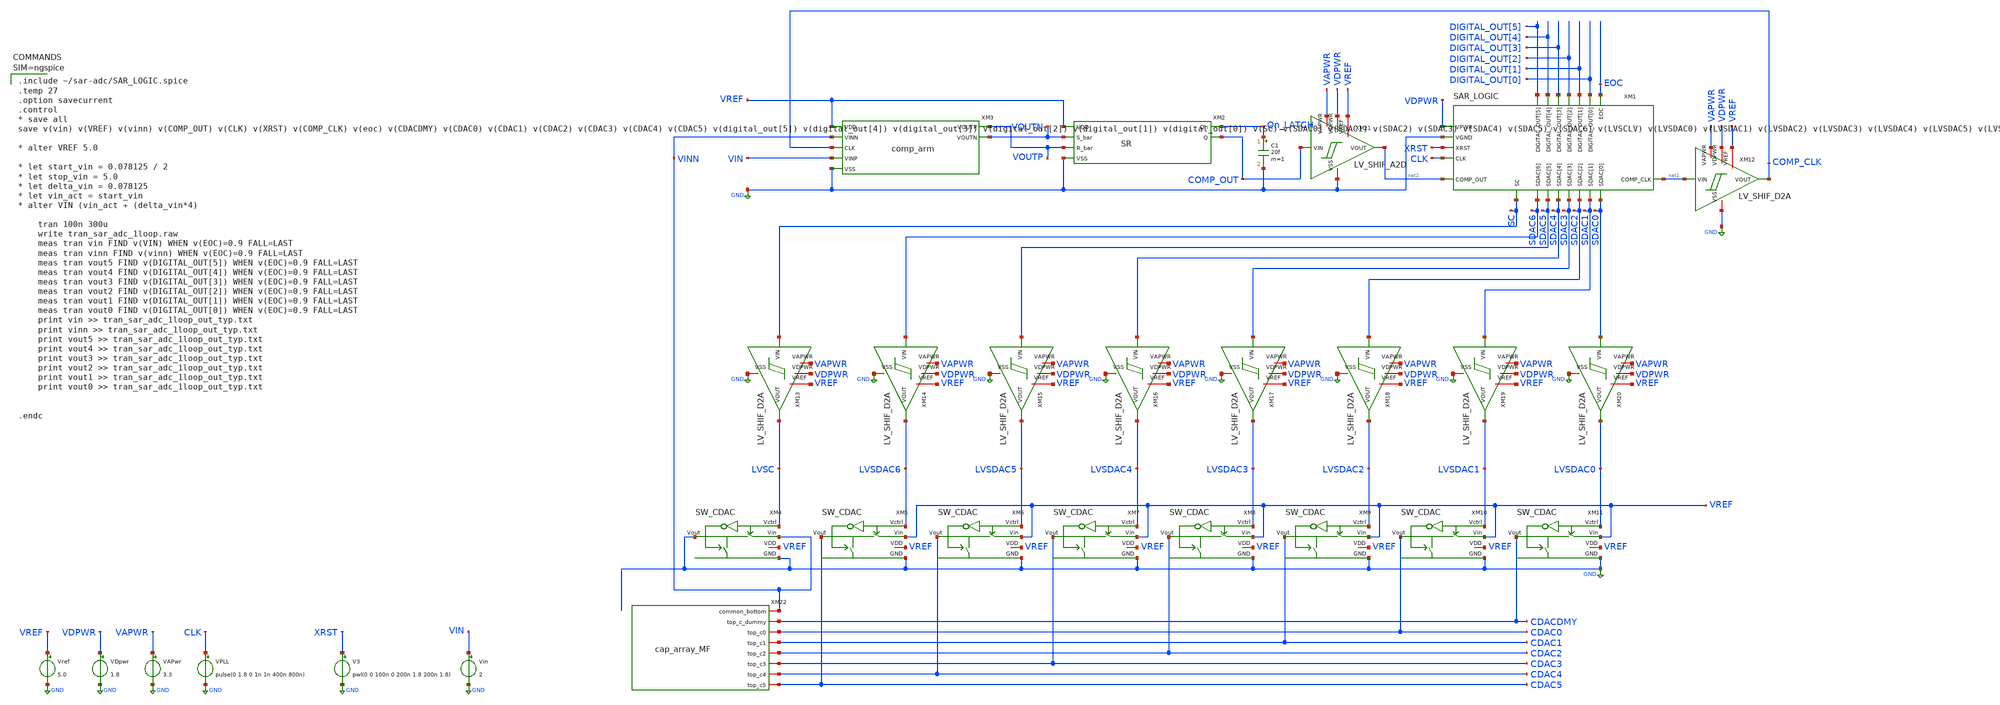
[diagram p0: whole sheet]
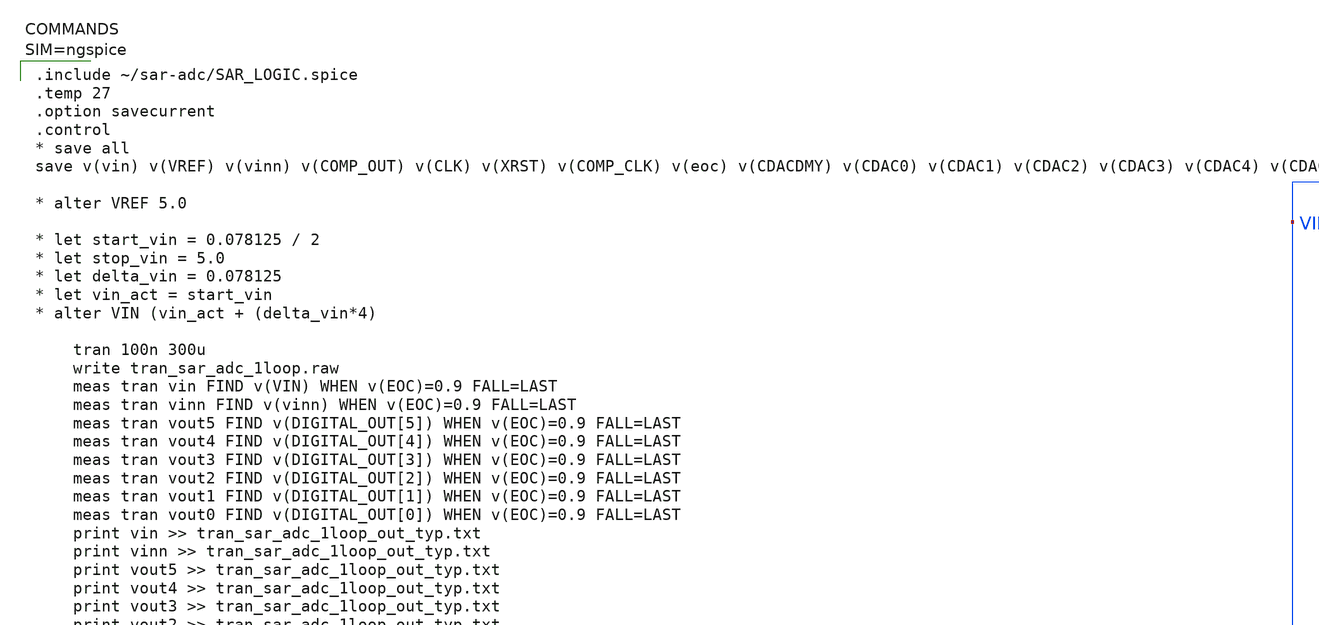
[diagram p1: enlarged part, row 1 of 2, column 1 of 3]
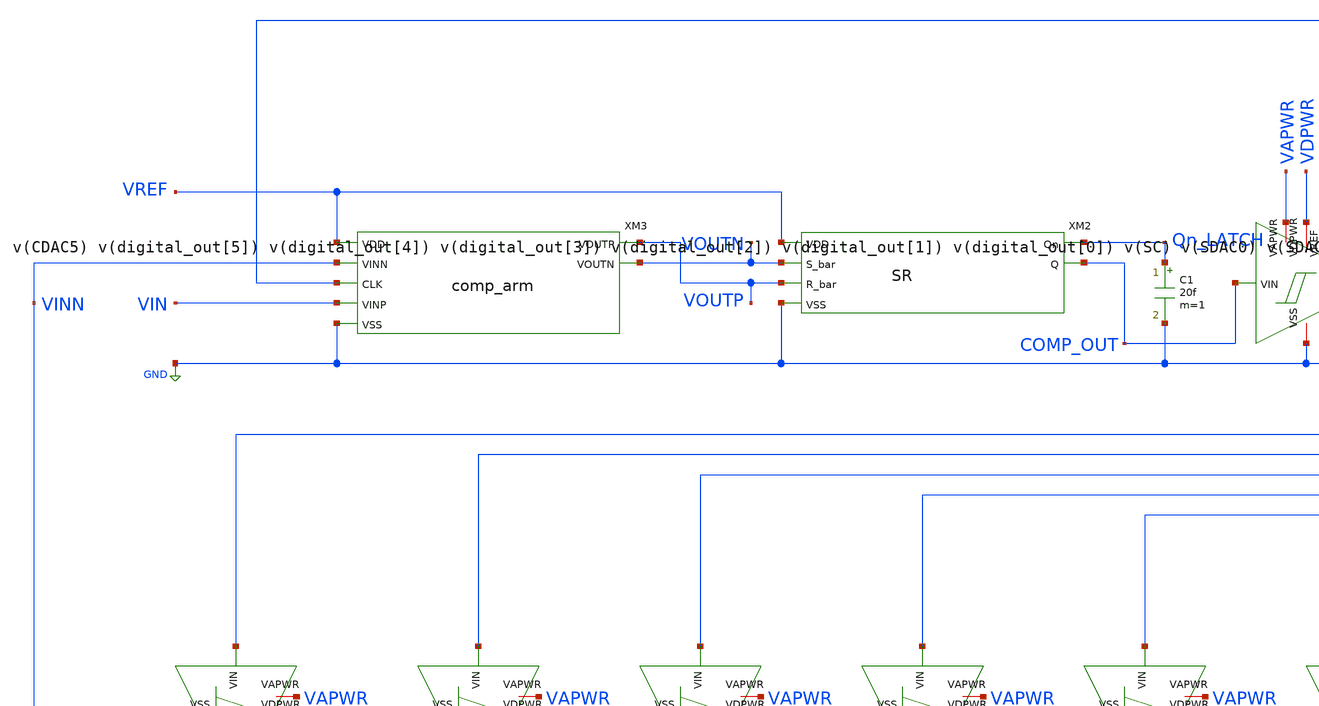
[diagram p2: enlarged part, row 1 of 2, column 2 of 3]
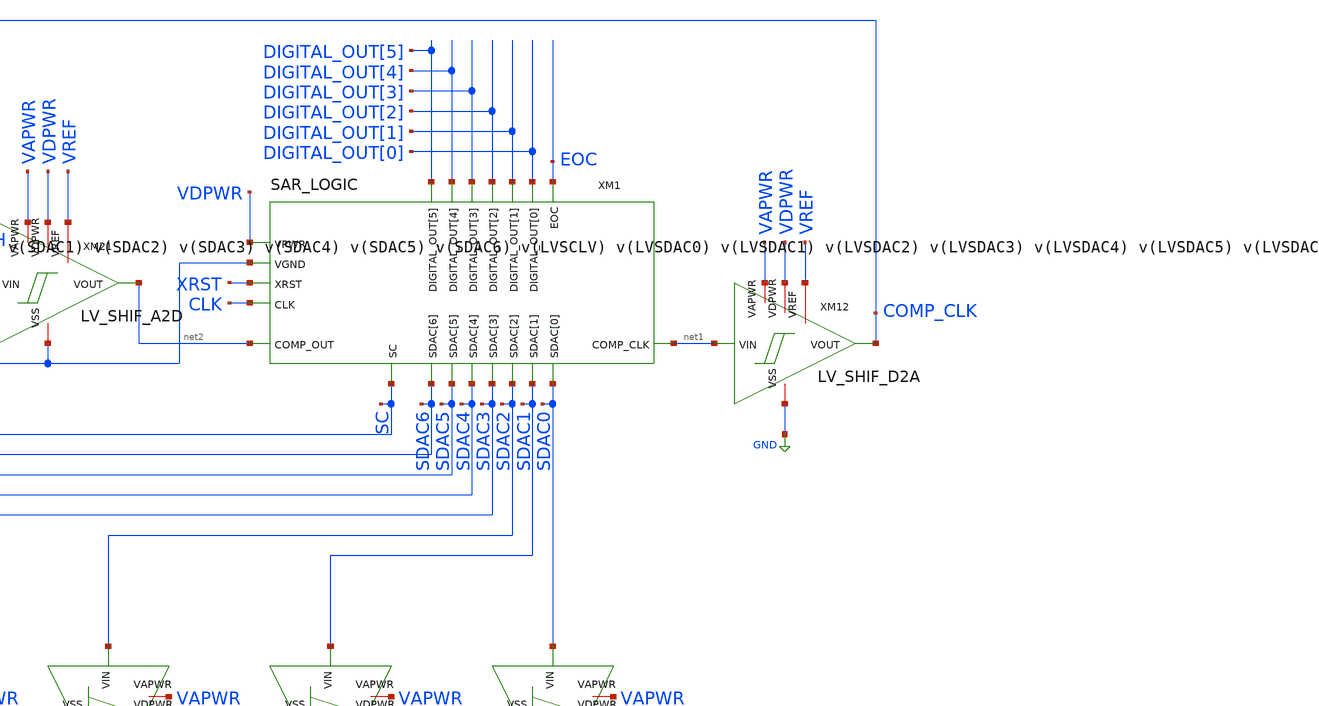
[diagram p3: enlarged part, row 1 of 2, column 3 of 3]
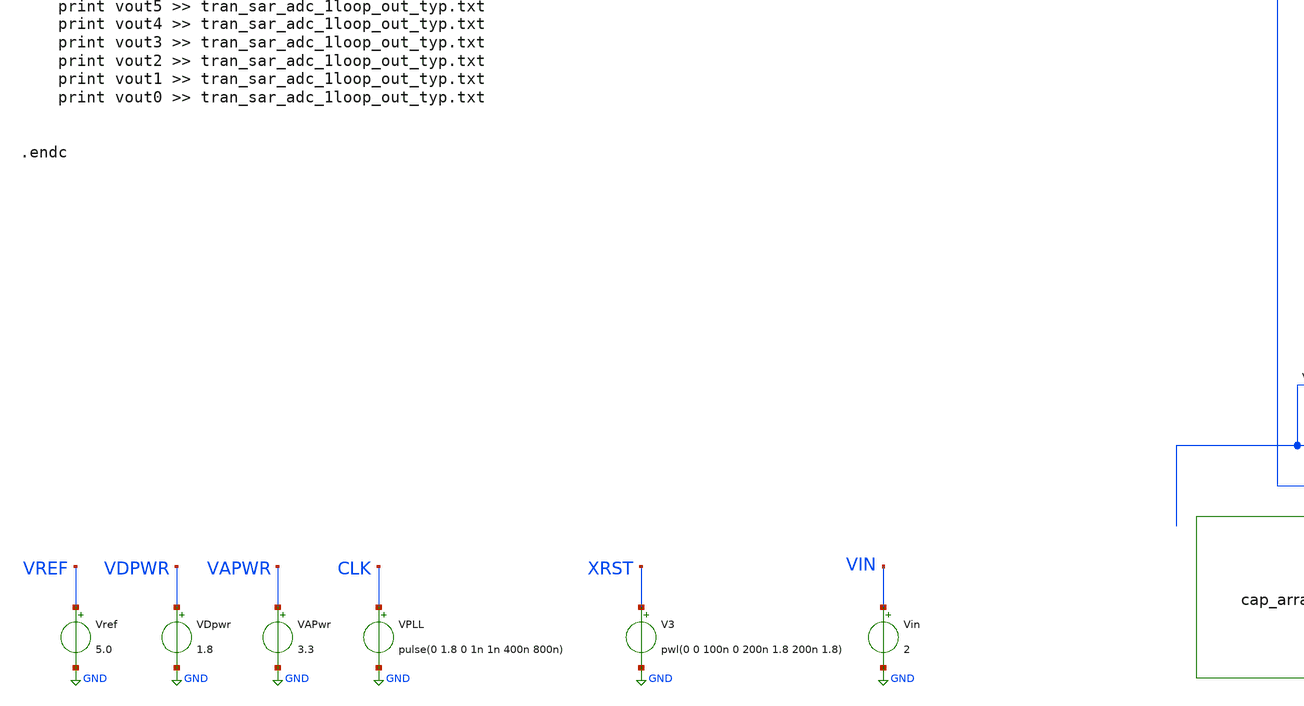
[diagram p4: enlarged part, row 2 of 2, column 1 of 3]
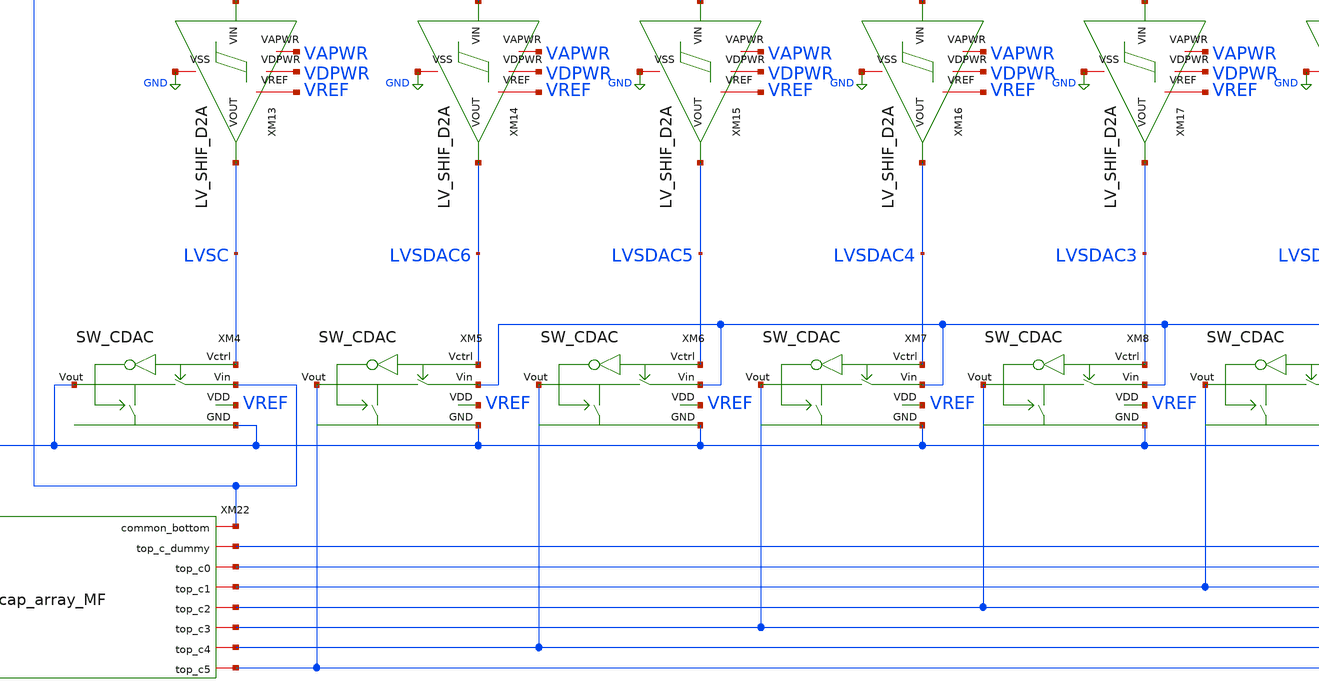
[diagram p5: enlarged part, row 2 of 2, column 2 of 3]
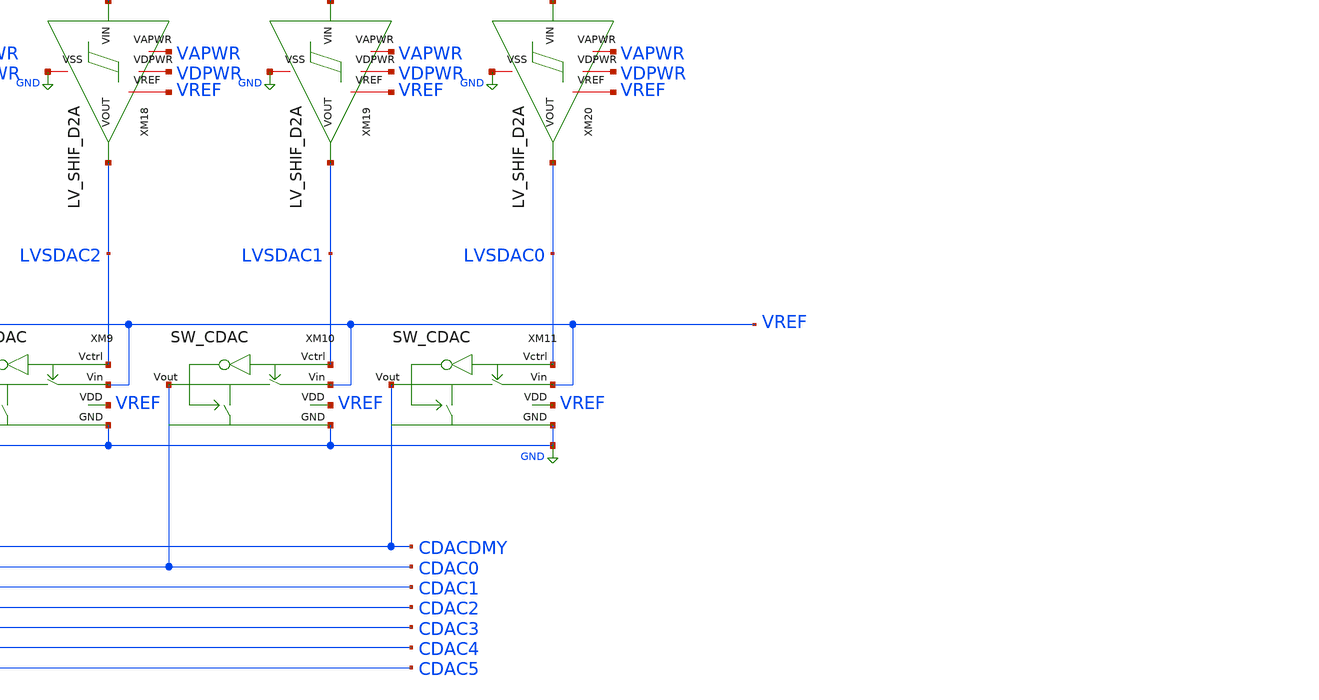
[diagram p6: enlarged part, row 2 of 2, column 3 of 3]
** sch_path: xschem/tran_sar_adc_1loop_arm.sch
**.subckt tran_sar_adc_1loop_arm
VAPwr VAPWR GND 3.3
Vin VIN GND 2
Vref VREF GND 5.0
VDpwr VDPWR GND 1.8
XXM2 VREF Qn_LATCH COMP_OUT VOUTP VOUTN GND SR
XM1 CLK net1 net2 DIGITAL_OUT[0] DIGITAL_OUT[1] DIGITAL_OUT[2] DIGITAL_OUT[3] DIGITAL_OUT[4]
+ DIGITAL_OUT[5] EOC SC SDAC0 SDAC1 SDAC2 SDAC3 SDAC4 SDAC5 SDAC6 GND VDPWR XRST SAR_LOGIC
XXM4 VREF LVSC GND GND VINN SW_CDAC
XXM5 VREF LVSDAC6 GND CDAC5 VREF SW_CDAC
XXM6 VREF LVSDAC5 GND CDAC4 VREF SW_CDAC
XXM7 VREF LVSDAC4 GND CDAC3 VREF SW_CDAC
XXM8 VREF LVSDAC3 GND CDAC2 VREF SW_CDAC
XXM9 VREF LVSDAC2 GND CDAC1 VREF SW_CDAC
XXM10 VREF LVSDAC1 GND CDAC0 VREF SW_CDAC
XXM11 VREF LVSDAC0 GND CDACDMY VREF SW_CDAC
XXM12 VAPWR VDPWR VREF COMP_CLK net1 GND LV_SHIF_D2A
XXM13 VAPWR VDPWR VREF LVSC SC GND LV_SHIF_D2A
XXM14 VAPWR VDPWR VREF LVSDAC6 SDAC6 GND LV_SHIF_D2A
XXM15 VAPWR VDPWR VREF LVSDAC5 SDAC5 GND LV_SHIF_D2A
XXM16 VAPWR VDPWR VREF LVSDAC4 SDAC4 GND LV_SHIF_D2A
XXM17 VAPWR VDPWR VREF LVSDAC3 SDAC3 GND LV_SHIF_D2A
XXM18 VAPWR VDPWR VREF LVSDAC2 SDAC2 GND LV_SHIF_D2A
XXM19 VAPWR VDPWR VREF LVSDAC1 SDAC1 GND LV_SHIF_D2A
XXM20 VAPWR VDPWR VREF LVSDAC0 SDAC0 GND LV_SHIF_D2A
XXM21 VAPWR VDPWR VREF net2 COMP_OUT GND LV_SHIF_A2D
XXM22 VINN CDAC5 CDAC0 CDAC2 CDAC4 CDAC3 CDACDMY CDAC1 cap_array_MF
VPLL CLK GND pulse(0 1.8 0 1n 1n 400n 800n)
V3 XRST GND pwl(0 0 100n 0 200n 1.8 200n 1.8)
XXM3 VOUTP VREF VIN VINN COMP_CLK GND VOUTN comp_arm
C1 Qn_LATCH GND 20f m=1
**** begin user architecture code


.include ~/sar-adc/SAR_LOGIC.spice
.temp 27
.option savecurrent
.control
* save all
save v(vin) v(VREF) v(vinn) v(COMP_OUT) v(CLK) v(XRST) v(COMP_CLK) v(eoc) v(CDACDMY) v(CDAC0)
+ v(CDAC1) v(CDAC2) v(CDAC3) v(CDAC4) v(CDAC5) v(digital_out[5]) v(digital_out[4]) v(digital_out[3])
+ v(digital_out[2]) v(digital_out[1]) v(digital_out[0]) v(SC) v(SDAC0) v(SDAC1) v(SDAC2) v(SDAC3) v(SDAC4) v(SDAC5)
+ v(SDAC6) v(LVSCLV) v(LVSDAC0) v(LVSDAC1) v(LVSDAC2) v(LVSDAC3) v(LVSDAC4) v(LVSDAC5) v(LVSDAC6)

* alter VREF 5.0

* let start_vin = 0.078125 / 2
* let stop_vin = 5.0
* let delta_vin = 0.078125
* let vin_act = start_vin
* alter VIN (vin_act + (delta_vin*4)

	tran 100n 300u
	write tran_sar_adc_1loop.raw
	meas tran vin FIND v(VIN) WHEN v(EOC)=0.9 FALL=LAST
	meas tran vinn FIND v(vinn) WHEN v(EOC)=0.9 FALL=LAST
	meas tran vout5 FIND v(DIGITAL_OUT[5]) WHEN v(EOC)=0.9 FALL=LAST
	meas tran vout4 FIND v(DIGITAL_OUT[4]) WHEN v(EOC)=0.9 FALL=LAST
	meas tran vout3 FIND v(DIGITAL_OUT[3]) WHEN v(EOC)=0.9 FALL=LAST
	meas tran vout2 FIND v(DIGITAL_OUT[2]) WHEN v(EOC)=0.9 FALL=LAST
	meas tran vout1 FIND v(DIGITAL_OUT[1]) WHEN v(EOC)=0.9 FALL=LAST
	meas tran vout0 FIND v(DIGITAL_OUT[0]) WHEN v(EOC)=0.9 FALL=LAST
	print vin >> tran_sar_adc_1loop_out_typ.txt
	print vinn >> tran_sar_adc_1loop_out_typ.txt
	print vout5 >> tran_sar_adc_1loop_out_typ.txt
	print vout4 >> tran_sar_adc_1loop_out_typ.txt
	print vout3 >> tran_sar_adc_1loop_out_typ.txt
	print vout2 >> tran_sar_adc_1loop_out_typ.txt
	print vout1 >> tran_sar_adc_1loop_out_typ.txt
	print vout0 >> tran_sar_adc_1loop_out_typ.txt


.endc




** opencircuitdesign pdks install
.lib $::SKYWATER_MODELS/sky130.lib.spice tt

**** end user architecture code
**.ends

* expanding   symbol:  SR.sym # of pins=6
** sym_path: xschem/SR.sym
** sch_path: xschem/SR.sch
.subckt SR VDD Qn Q R_bar S_bar VSS


*.iopin VDD
*.opin Qn
*.opin Q
*.ipin S_bar
*.ipin R_bar
*.iopin VSS
XM7 Q Qn VDD VDD sky130_fd_pr__pfet_g5v0d10v5 L=0.5 W=6 nf=1 ad='int((1 + 1)/2) * 6 / 1 * 0.29' as='int((1 + 2)/2) * 6 / 1 * 0.29'
+ pd='2*int((1 + 1)/2) * (6 / 1 + 0.29)' ps='2*int((1 + 2)/2) * (6 / 1 + 0.29)' nrd='0.29 / 6 ' nrs='0.29 / 6 '
+ sa=0 sb=0 sd=0 mult=1 m=1
XM8 Q S_bar VDD VDD sky130_fd_pr__pfet_g5v0d10v5 L=0.5 W=6 nf=1 ad='int((1 + 1)/2) * 6 / 1 * 0.29' as='int((1 + 2)/2) * 6 / 1 * 0.29'
+ pd='2*int((1 + 1)/2) * (6 / 1 + 0.29)' ps='2*int((1 + 2)/2) * (6 / 1 + 0.29)' nrd='0.29 / 6 ' nrs='0.29 / 6 '
+ sa=0 sb=0 sd=0 mult=1 m=1
XM15 Q S_bar net1 VSS sky130_fd_pr__nfet_g5v0d10v5 L=0.5 W=3 nf=1 ad='int((1 + 1)/2) * 3 / 1 * 0.29'
+ as='int((1 + 2)/2) * 3 / 1 * 0.29' pd='2*int((1 + 1)/2) * (3 / 1 + 0.29)' ps='2*int((1 + 2)/2) * (3 / 1 + 0.29)'
+ nrd='0.29 / 3 ' nrs='0.29 / 3 ' sa=0 sb=0 sd=0 mult=1 m=1
XM16 net1 Qn VSS VSS sky130_fd_pr__nfet_g5v0d10v5 L=0.5 W=3 nf=1 ad='int((1 + 1)/2) * 3 / 1 * 0.29' as='int((1 + 2)/2) * 3 / 1 * 0.29'
+ pd='2*int((1 + 1)/2) * (3 / 1 + 0.29)' ps='2*int((1 + 2)/2) * (3 / 1 + 0.29)' nrd='0.29 / 3 ' nrs='0.29 / 3 '
+ sa=0 sb=0 sd=0 mult=1 m=1
XM17 Qn R_bar VDD VDD sky130_fd_pr__pfet_g5v0d10v5 L=0.5 W=6 nf=1 ad='int((1 + 1)/2) * 6 / 1 * 0.29'
+ as='int((1 + 2)/2) * 6 / 1 * 0.29' pd='2*int((1 + 1)/2) * (6 / 1 + 0.29)' ps='2*int((1 + 2)/2) * (6 / 1 + 0.29)'
+ nrd='0.29 / 6 ' nrs='0.29 / 6 ' sa=0 sb=0 sd=0 mult=1 m=1
XM18 Qn Q VDD VDD sky130_fd_pr__pfet_g5v0d10v5 L=0.5 W=6 nf=1 ad='int((1 + 1)/2) * 6 / 1 * 0.29' as='int((1 + 2)/2) * 6 / 1 * 0.29'
+ pd='2*int((1 + 1)/2) * (6 / 1 + 0.29)' ps='2*int((1 + 2)/2) * (6 / 1 + 0.29)' nrd='0.29 / 6 ' nrs='0.29 / 6 '
+ sa=0 sb=0 sd=0 mult=1 m=1
XM23 Qn Q net2 VSS sky130_fd_pr__nfet_g5v0d10v5 L=0.5 W=3 nf=1 ad='int((1 + 1)/2) * 3 / 1 * 0.29' as='int((1 + 2)/2) * 3 / 1 * 0.29'
+ pd='2*int((1 + 1)/2) * (3 / 1 + 0.29)' ps='2*int((1 + 2)/2) * (3 / 1 + 0.29)' nrd='0.29 / 3 ' nrs='0.29 / 3 '
+ sa=0 sb=0 sd=0 mult=1 m=1
XM27 net2 R_bar VSS VSS sky130_fd_pr__nfet_g5v0d10v5 L=0.5 W=3 nf=1 ad='int((1 + 1)/2) * 3 / 1 * 0.29'
+ as='int((1 + 2)/2) * 3 / 1 * 0.29' pd='2*int((1 + 1)/2) * (3 / 1 + 0.29)' ps='2*int((1 + 2)/2) * (3 / 1 + 0.29)'
+ nrd='0.29 / 3 ' nrs='0.29 / 3 ' sa=0 sb=0 sd=0 mult=1 m=1
.ends


* expanding   symbol:  SW_CDAC.sym # of pins=5
** sym_path: xschem/SW_CDAC.sym
** sch_path: xschem/SW_CDAC.sch
.subckt SW_CDAC VDD Vctrl GND Vout Vin

*.ipin Vctrl
*.ipin Vin
*.opin Vout
*.ipin VDD
*.ipin GND
XM1 Vin net1 Vout VDD sky130_fd_pr__pfet_g5v0d10v5 L=0.5 W=60 nf=1 ad='int((1 + 1)/2) * 60 / 1 * 0.29'
+ as='int((1 + 2)/2) * 60 / 1 * 0.29' pd='2*int((1 + 1)/2) * (60 / 1 + 0.29)' ps='2*int((1 + 2)/2) * (60 / 1 + 0.29)'
+ nrd='0.29 / 60 ' nrs='0.29 / 60 ' sa=0 sb=0 sd=0 mult=1 m=1
XM2 Vin Vctrl Vout GND sky130_fd_pr__nfet_g5v0d10v5 L=0.5 W=30 nf=1 ad='int((1 + 1)/2) * 30 / 1 * 0.29'
+ as='int((1 + 2)/2) * 30 / 1 * 0.29' pd='2*int((1 + 1)/2) * (30 / 1 + 0.29)' ps='2*int((1 + 2)/2) * (30 / 1 + 0.29)'
+ nrd='0.29 / 30 ' nrs='0.29 / 30 ' sa=0 sb=0 sd=0 mult=1 m=1
XM3 net1 Vctrl VDD VDD sky130_fd_pr__pfet_g5v0d10v5 L=0.5 W=60 nf=1 ad='int((1 + 1)/2) * 60 / 1 * 0.29'
+ as='int((1 + 2)/2) * 60 / 1 * 0.29' pd='2*int((1 + 1)/2) * (60 / 1 + 0.29)' ps='2*int((1 + 2)/2) * (60 / 1 + 0.29)'
+ nrd='0.29 / 60 ' nrs='0.29 / 60 ' sa=0 sb=0 sd=0 mult=1 m=1
XM4 net1 Vctrl GND GND sky130_fd_pr__nfet_g5v0d10v5 L=0.5 W=30 nf=1 ad='int((1 + 1)/2) * 30 / 1 * 0.29'
+ as='int((1 + 2)/2) * 30 / 1 * 0.29' pd='2*int((1 + 1)/2) * (30 / 1 + 0.29)' ps='2*int((1 + 2)/2) * (30 / 1 + 0.29)'
+ nrd='0.29 / 30 ' nrs='0.29 / 30 ' sa=0 sb=0 sd=0 mult=1 m=1
XM5 Vout net1 GND GND sky130_fd_pr__nfet_g5v0d10v5 L=0.5 W=30 nf=1 ad='int((1 + 1)/2) * 30 / 1 * 0.29'
+ as='int((1 + 2)/2) * 30 / 1 * 0.29' pd='2*int((1 + 1)/2) * (30 / 1 + 0.29)' ps='2*int((1 + 2)/2) * (30 / 1 + 0.29)'
+ nrd='0.29 / 30 ' nrs='0.29 / 30 ' sa=0 sb=0 sd=0 mult=1 m=1
.ends


* expanding   symbol:  LV_SHIF_D2A.sym # of pins=6
** sym_path: xschem/LV_SHIF_D2A.sym
** sch_path: xschem/LV_SHIF_D2A.sch
.subckt LV_SHIF_D2A VAPWR VDPWR VREF VOUT VIN VSS


*.iopin VDPWR
*.iopin VSS
*.iopin VAPWR
*.iopin VREF
*.ipin VIN
*.opin VOUT
XM2 net1 VIN VSS VSS sky130_fd_pr__nfet_g5v0d10v5 L=0.5 W=2 nf=1 ad='int((1 + 1)/2) * 2 / 1 * 0.29' as='int((1 + 2)/2) * 2 / 1 * 0.29'
+ pd='2*int((1 + 1)/2) * (2 / 1 + 0.29)' ps='2*int((1 + 2)/2) * (2 / 1 + 0.29)' nrd='0.29 / 2 ' nrs='0.29 / 2 '
+ sa=0 sb=0 sd=0 mult=1 m=1
XM1 net1 VIN VDPWR VDPWR sky130_fd_pr__pfet_g5v0d10v5 L=0.5 W=5 nf=1 ad='int((1 + 1)/2) * 5 / 1 * 0.29'
+ as='int((1 + 2)/2) * 5 / 1 * 0.29' pd='2*int((1 + 1)/2) * (5 / 1 + 0.29)' ps='2*int((1 + 2)/2) * (5 / 1 + 0.29)'
+ nrd='0.29 / 5 ' nrs='0.29 / 5 ' sa=0 sb=0 sd=0 mult=1 m=1
XM3 net2 net1 VSS VSS sky130_fd_pr__nfet_g5v0d10v5 L=0.5 W=2 nf=1 ad='int((1 + 1)/2) * 2 / 1 * 0.29'
+ as='int((1 + 2)/2) * 2 / 1 * 0.29' pd='2*int((1 + 1)/2) * (2 / 1 + 0.29)' ps='2*int((1 + 2)/2) * (2 / 1 + 0.29)'
+ nrd='0.29 / 2 ' nrs='0.29 / 2 ' sa=0 sb=0 sd=0 mult=1 m=1
XM4 net2 net1 VDPWR VDPWR sky130_fd_pr__pfet_g5v0d10v5 L=0.5 W=5 nf=1 ad='int((1 + 1)/2) * 5 / 1 * 0.29'
+ as='int((1 + 2)/2) * 5 / 1 * 0.29' pd='2*int((1 + 1)/2) * (5 / 1 + 0.29)' ps='2*int((1 + 2)/2) * (5 / 1 + 0.29)'
+ nrd='0.29 / 5 ' nrs='0.29 / 5 ' sa=0 sb=0 sd=0 mult=1 m=1
XM5 net3 net2 VSS VSS sky130_fd_pr__nfet_g5v0d10v5 L=0.5 W=4 nf=1 ad='int((1 + 1)/2) * 4 / 1 * 0.29'
+ as='int((1 + 2)/2) * 4 / 1 * 0.29' pd='2*int((1 + 1)/2) * (4 / 1 + 0.29)' ps='2*int((1 + 2)/2) * (4 / 1 + 0.29)'
+ nrd='0.29 / 4 ' nrs='0.29 / 4 ' sa=0 sb=0 sd=0 mult=1 m=1
XM6 net3 net2 VAPWR VAPWR sky130_fd_pr__pfet_g5v0d10v5 L=0.5 W=10 nf=1 ad='int((1 + 1)/2) * 10 / 1 * 0.29'
+ as='int((1 + 2)/2) * 10 / 1 * 0.29' pd='2*int((1 + 1)/2) * (10 / 1 + 0.29)' ps='2*int((1 + 2)/2) * (10 / 1 + 0.29)'
+ nrd='0.29 / 10 ' nrs='0.29 / 10 ' sa=0 sb=0 sd=0 mult=1 m=1
XM7 net4 net3 VSS VSS sky130_fd_pr__nfet_g5v0d10v5 L=0.5 W=4 nf=1 ad='int((1 + 1)/2) * 4 / 1 * 0.29'
+ as='int((1 + 2)/2) * 4 / 1 * 0.29' pd='2*int((1 + 1)/2) * (4 / 1 + 0.29)' ps='2*int((1 + 2)/2) * (4 / 1 + 0.29)'
+ nrd='0.29 / 4 ' nrs='0.29 / 4 ' sa=0 sb=0 sd=0 mult=1 m=1
XM8 net4 net3 VAPWR VAPWR sky130_fd_pr__pfet_g5v0d10v5 L=0.5 W=10 nf=1 ad='int((1 + 1)/2) * 10 / 1 * 0.29'
+ as='int((1 + 2)/2) * 10 / 1 * 0.29' pd='2*int((1 + 1)/2) * (10 / 1 + 0.29)' ps='2*int((1 + 2)/2) * (10 / 1 + 0.29)'
+ nrd='0.29 / 10 ' nrs='0.29 / 10 ' sa=0 sb=0 sd=0 mult=1 m=1
XM9 net5 net4 VSS VSS sky130_fd_pr__nfet_g5v0d10v5 L=0.5 W=8 nf=1 ad='int((1 + 1)/2) * 8 / 1 * 0.29'
+ as='int((1 + 2)/2) * 8 / 1 * 0.29' pd='2*int((1 + 1)/2) * (8 / 1 + 0.29)' ps='2*int((1 + 2)/2) * (8 / 1 + 0.29)'
+ nrd='0.29 / 8 ' nrs='0.29 / 8 ' sa=0 sb=0 sd=0 mult=1 m=1
XM10 net5 net4 VREF VREF sky130_fd_pr__pfet_g5v0d10v5 L=0.5 W=20 nf=1 ad='int((1 + 1)/2) * 20 / 1 * 0.29'
+ as='int((1 + 2)/2) * 20 / 1 * 0.29' pd='2*int((1 + 1)/2) * (20 / 1 + 0.29)' ps='2*int((1 + 2)/2) * (20 / 1 + 0.29)'
+ nrd='0.29 / 20 ' nrs='0.29 / 20 ' sa=0 sb=0 sd=0 mult=1 m=1
XM11 VOUT net5 VSS VSS sky130_fd_pr__nfet_g5v0d10v5 L=0.5 W=8 nf=1 ad='int((1 + 1)/2) * 8 / 1 * 0.29'
+ as='int((1 + 2)/2) * 8 / 1 * 0.29' pd='2*int((1 + 1)/2) * (8 / 1 + 0.29)' ps='2*int((1 + 2)/2) * (8 / 1 + 0.29)'
+ nrd='0.29 / 8 ' nrs='0.29 / 8 ' sa=0 sb=0 sd=0 mult=1 m=1
XM12 VOUT net5 VREF VREF sky130_fd_pr__pfet_g5v0d10v5 L=0.5 W=20 nf=1 ad='int((1 + 1)/2) * 20 / 1 * 0.29'
+ as='int((1 + 2)/2) * 20 / 1 * 0.29' pd='2*int((1 + 1)/2) * (20 / 1 + 0.29)' ps='2*int((1 + 2)/2) * (20 / 1 + 0.29)'
+ nrd='0.29 / 20 ' nrs='0.29 / 20 ' sa=0 sb=0 sd=0 mult=1 m=1
.ends


* expanding   symbol:  LV_SHIF_A2D.sym # of pins=6
** sym_path: LV_SHIF_A2D.sym
** sch_path: LV_SHIF_A2D.sch
.subckt LV_SHIF_A2D VAPWR VDPWR VREF VOUT VIN VSS


*.iopin VDPWR
*.iopin VSS
*.iopin VAPWR
*.iopin VREF
*.ipin VIN
*.opin VOUT
XM2 net1 VIN VSS VSS sky130_fd_pr__nfet_g5v0d10v5 L=0.5 W=2 nf=1 ad='int((1 + 1)/2) * 2 / 1 * 0.29' as='int((1 + 2)/2) * 2 / 1 * 0.29'
+ pd='2*int((1 + 1)/2) * (2 / 1 + 0.29)' ps='2*int((1 + 2)/2) * (2 / 1 + 0.29)' nrd='0.29 / 2 ' nrs='0.29 / 2 '
+ sa=0 sb=0 sd=0 mult=1 m=1
XM1 net1 VIN VREF VREF sky130_fd_pr__pfet_g5v0d10v5 L=0.5 W=5 nf=1 ad='int((1 + 1)/2) * 5 / 1 * 0.29'
+ as='int((1 + 2)/2) * 5 / 1 * 0.29' pd='2*int((1 + 1)/2) * (5 / 1 + 0.29)' ps='2*int((1 + 2)/2) * (5 / 1 + 0.29)'
+ nrd='0.29 / 5 ' nrs='0.29 / 5 ' sa=0 sb=0 sd=0 mult=1 m=1
XM3 net2 net1 VSS VSS sky130_fd_pr__nfet_g5v0d10v5 L=0.5 W=2 nf=1 ad='int((1 + 1)/2) * 2 / 1 * 0.29'
+ as='int((1 + 2)/2) * 2 / 1 * 0.29' pd='2*int((1 + 1)/2) * (2 / 1 + 0.29)' ps='2*int((1 + 2)/2) * (2 / 1 + 0.29)'
+ nrd='0.29 / 2 ' nrs='0.29 / 2 ' sa=0 sb=0 sd=0 mult=1 m=1
XM4 net2 net1 VREF VREF sky130_fd_pr__pfet_g5v0d10v5 L=0.5 W=5 nf=1 ad='int((1 + 1)/2) * 5 / 1 * 0.29'
+ as='int((1 + 2)/2) * 5 / 1 * 0.29' pd='2*int((1 + 1)/2) * (5 / 1 + 0.29)' ps='2*int((1 + 2)/2) * (5 / 1 + 0.29)'
+ nrd='0.29 / 5 ' nrs='0.29 / 5 ' sa=0 sb=0 sd=0 mult=1 m=1
XM5 net3 net2 VSS VSS sky130_fd_pr__nfet_g5v0d10v5 L=0.5 W=4 nf=1 ad='int((1 + 1)/2) * 4 / 1 * 0.29'
+ as='int((1 + 2)/2) * 4 / 1 * 0.29' pd='2*int((1 + 1)/2) * (4 / 1 + 0.29)' ps='2*int((1 + 2)/2) * (4 / 1 + 0.29)'
+ nrd='0.29 / 4 ' nrs='0.29 / 4 ' sa=0 sb=0 sd=0 mult=1 m=1
XM6 net3 net2 VAPWR VAPWR sky130_fd_pr__pfet_g5v0d10v5 L=0.5 W=10 nf=1 ad='int((1 + 1)/2) * 10 / 1 * 0.29'
+ as='int((1 + 2)/2) * 10 / 1 * 0.29' pd='2*int((1 + 1)/2) * (10 / 1 + 0.29)' ps='2*int((1 + 2)/2) * (10 / 1 + 0.29)'
+ nrd='0.29 / 10 ' nrs='0.29 / 10 ' sa=0 sb=0 sd=0 mult=1 m=1
XM7 net4 net3 VSS VSS sky130_fd_pr__nfet_g5v0d10v5 L=0.5 W=4 nf=1 ad='int((1 + 1)/2) * 4 / 1 * 0.29'
+ as='int((1 + 2)/2) * 4 / 1 * 0.29' pd='2*int((1 + 1)/2) * (4 / 1 + 0.29)' ps='2*int((1 + 2)/2) * (4 / 1 + 0.29)'
+ nrd='0.29 / 4 ' nrs='0.29 / 4 ' sa=0 sb=0 sd=0 mult=1 m=1
XM8 net4 net3 VAPWR VAPWR sky130_fd_pr__pfet_g5v0d10v5 L=0.5 W=10 nf=1 ad='int((1 + 1)/2) * 10 / 1 * 0.29'
+ as='int((1 + 2)/2) * 10 / 1 * 0.29' pd='2*int((1 + 1)/2) * (10 / 1 + 0.29)' ps='2*int((1 + 2)/2) * (10 / 1 + 0.29)'
+ nrd='0.29 / 10 ' nrs='0.29 / 10 ' sa=0 sb=0 sd=0 mult=1 m=1
XM9 net5 net4 VSS VSS sky130_fd_pr__nfet_g5v0d10v5 L=0.5 W=8 nf=1 ad='int((1 + 1)/2) * 8 / 1 * 0.29'
+ as='int((1 + 2)/2) * 8 / 1 * 0.29' pd='2*int((1 + 1)/2) * (8 / 1 + 0.29)' ps='2*int((1 + 2)/2) * (8 / 1 + 0.29)'
+ nrd='0.29 / 8 ' nrs='0.29 / 8 ' sa=0 sb=0 sd=0 mult=1 m=1
XM10 net5 net4 VDPWR VDPWR sky130_fd_pr__pfet_g5v0d10v5 L=0.5 W=20 nf=1 ad='int((1 + 1)/2) * 20 / 1 * 0.29'
+ as='int((1 + 2)/2) * 20 / 1 * 0.29' pd='2*int((1 + 1)/2) * (20 / 1 + 0.29)' ps='2*int((1 + 2)/2) * (20 / 1 + 0.29)'
+ nrd='0.29 / 20 ' nrs='0.29 / 20 ' sa=0 sb=0 sd=0 mult=1 m=1
XM11 VOUT net5 VSS VSS sky130_fd_pr__nfet_g5v0d10v5 L=0.5 W=8 nf=1 ad='int((1 + 1)/2) * 8 / 1 * 0.29'
+ as='int((1 + 2)/2) * 8 / 1 * 0.29' pd='2*int((1 + 1)/2) * (8 / 1 + 0.29)' ps='2*int((1 + 2)/2) * (8 / 1 + 0.29)'
+ nrd='0.29 / 8 ' nrs='0.29 / 8 ' sa=0 sb=0 sd=0 mult=1 m=1
XM12 VOUT net5 VDPWR VDPWR sky130_fd_pr__pfet_g5v0d10v5 L=0.5 W=20 nf=1 ad='int((1 + 1)/2) * 20 / 1 * 0.29'
+ as='int((1 + 2)/2) * 20 / 1 * 0.29' pd='2*int((1 + 1)/2) * (20 / 1 + 0.29)' ps='2*int((1 + 2)/2) * (20 / 1 + 0.29)'
+ nrd='0.29 / 20 ' nrs='0.29 / 20 ' sa=0 sb=0 sd=0 mult=1 m=1
.ends


* expanding   symbol:  cap_array_MF.sym # of pins=8
** sym_path: xschem/cap_array_MF.sym
** sch_path: xschem/cap_array_MF.sch
.subckt cap_array_MF common_bottom top_c5 top_c0 top_c2 top_c4 top_c3 top_c_dummy top_c1

*.iopin common_bottom
*.iopin top_c1
*.iopin top_c0
*.iopin top_c_dummy
*.iopin top_c2
*.iopin top_c4
*.iopin top_c5
*.iopin top_c3
Cdum top_c_dummy common_bottom 100f m=1
C0 top_c0 common_bottom 100f m=1
C1 top_c1 common_bottom 200f m=1
C2 top_c2 common_bottom 400f m=1
C3 top_c3 common_bottom 800f m=1
C4 top_c4 common_bottom 1600f m=1
C5 top_c5 common_bottom 3200f m=1
.ends


* expanding   symbol:  comp_arm.sym # of pins=7
** sym_path: xschem/comp_arm.sym
** sch_path: xschem/comp_arm.sch
.subckt comp_arm VOUTP VDD VINP VINN CLK VSS VOUTN

*.iopin VSS
*.iopin VDD
*.ipin CLK
*.ipin VINP
*.ipin VINN
*.opin VOUTN
*.opin VOUTP
XM1 net1 CLK VDD VDD sky130_fd_pr__pfet_g5v0d10v5 L=0.5 W=30 nf=1 ad='int((1 + 1)/2) * 30 / 1 * 0.29'
+ as='int((1 + 2)/2) * 30 / 1 * 0.29' pd='2*int((1 + 1)/2) * (30 / 1 + 0.29)' ps='2*int((1 + 2)/2) * (30 / 1 + 0.29)'
+ nrd='0.29 / 30 ' nrs='0.29 / 30 ' sa=0 sb=0 sd=0 mult=1 m=1
XM2 VOUTN CLK VDD VDD sky130_fd_pr__pfet_g5v0d10v5 L=0.5 W=30 nf=1 ad='int((1 + 1)/2) * 30 / 1 * 0.29'
+ as='int((1 + 2)/2) * 30 / 1 * 0.29' pd='2*int((1 + 1)/2) * (30 / 1 + 0.29)' ps='2*int((1 + 2)/2) * (30 / 1 + 0.29)'
+ nrd='0.29 / 30 ' nrs='0.29 / 30 ' sa=0 sb=0 sd=0 mult=1 m=1
XM3 VOUTN VOUTP VDD VDD sky130_fd_pr__pfet_g5v0d10v5 L=0.5 W=30 nf=1 ad='int((1 + 1)/2) * 30 / 1 * 0.29'
+ as='int((1 + 2)/2) * 30 / 1 * 0.29' pd='2*int((1 + 1)/2) * (30 / 1 + 0.29)' ps='2*int((1 + 2)/2) * (30 / 1 + 0.29)'
+ nrd='0.29 / 30 ' nrs='0.29 / 30 ' sa=0 sb=0 sd=0 mult=1 m=1
XM4 VOUTP VOUTN VDD VDD sky130_fd_pr__pfet_g5v0d10v5 L=0.5 W=30 nf=1 ad='int((1 + 1)/2) * 30 / 1 * 0.29'
+ as='int((1 + 2)/2) * 30 / 1 * 0.29' pd='2*int((1 + 1)/2) * (30 / 1 + 0.29)' ps='2*int((1 + 2)/2) * (30 / 1 + 0.29)'
+ nrd='0.29 / 30 ' nrs='0.29 / 30 ' sa=0 sb=0 sd=0 mult=1 m=1
XM5 VOUTP CLK VDD VDD sky130_fd_pr__pfet_g5v0d10v5 L=0.5 W=30 nf=1 ad='int((1 + 1)/2) * 30 / 1 * 0.29'
+ as='int((1 + 2)/2) * 30 / 1 * 0.29' pd='2*int((1 + 1)/2) * (30 / 1 + 0.29)' ps='2*int((1 + 2)/2) * (30 / 1 + 0.29)'
+ nrd='0.29 / 30 ' nrs='0.29 / 30 ' sa=0 sb=0 sd=0 mult=1 m=1
XM6 net2 CLK VDD VDD sky130_fd_pr__pfet_g5v0d10v5 L=0.5 W=30 nf=1 ad='int((1 + 1)/2) * 30 / 1 * 0.29'
+ as='int((1 + 2)/2) * 30 / 1 * 0.29' pd='2*int((1 + 1)/2) * (30 / 1 + 0.29)' ps='2*int((1 + 2)/2) * (30 / 1 + 0.29)'
+ nrd='0.29 / 30 ' nrs='0.29 / 30 ' sa=0 sb=0 sd=0 mult=1 m=1
XM7 VOUTN VOUTP net1 VSS sky130_fd_pr__nfet_g5v0d10v5 L=0.5 W=10 nf=1 ad='int((1 + 1)/2) * 10 / 1 * 0.29'
+ as='int((1 + 2)/2) * 10 / 1 * 0.29' pd='2*int((1 + 1)/2) * (10 / 1 + 0.29)' ps='2*int((1 + 2)/2) * (10 / 1 + 0.29)'
+ nrd='0.29 / 10 ' nrs='0.29 / 10 ' sa=0 sb=0 sd=0 mult=1 m=1
XM8 VOUTP VOUTN net2 VSS sky130_fd_pr__nfet_g5v0d10v5 L=0.5 W=10 nf=1 ad='int((1 + 1)/2) * 10 / 1 * 0.29'
+ as='int((1 + 2)/2) * 10 / 1 * 0.29' pd='2*int((1 + 1)/2) * (10 / 1 + 0.29)' ps='2*int((1 + 2)/2) * (10 / 1 + 0.29)'
+ nrd='0.29 / 10 ' nrs='0.29 / 10 ' sa=0 sb=0 sd=0 mult=1 m=1
XM9 net1 VINP net3 VSS sky130_fd_pr__nfet_g5v0d10v5 L=0.5 W=10 nf=1 ad='int((1 + 1)/2) * 10 / 1 * 0.29'
+ as='int((1 + 2)/2) * 10 / 1 * 0.29' pd='2*int((1 + 1)/2) * (10 / 1 + 0.29)' ps='2*int((1 + 2)/2) * (10 / 1 + 0.29)'
+ nrd='0.29 / 10 ' nrs='0.29 / 10 ' sa=0 sb=0 sd=0 mult=1 m=1
XM10 net2 VINN net3 VSS sky130_fd_pr__nfet_g5v0d10v5 L=0.5 W=10 nf=1 ad='int((1 + 1)/2) * 10 / 1 * 0.29'
+ as='int((1 + 2)/2) * 10 / 1 * 0.29' pd='2*int((1 + 1)/2) * (10 / 1 + 0.29)' ps='2*int((1 + 2)/2) * (10 / 1 + 0.29)'
+ nrd='0.29 / 10 ' nrs='0.29 / 10 ' sa=0 sb=0 sd=0 mult=1 m=1
XM11 net3 CLK VSS VSS sky130_fd_pr__nfet_g5v0d10v5 L=0.5 W=10 nf=1 ad='int((1 + 1)/2) * 10 / 1 * 0.29'
+ as='int((1 + 2)/2) * 10 / 1 * 0.29' pd='2*int((1 + 1)/2) * (10 / 1 + 0.29)' ps='2*int((1 + 2)/2) * (10 / 1 + 0.29)'
+ nrd='0.29 / 10 ' nrs='0.29 / 10 ' sa=0 sb=0 sd=0 mult=1 m=1
.ends

.GLOBAL GND
.end
